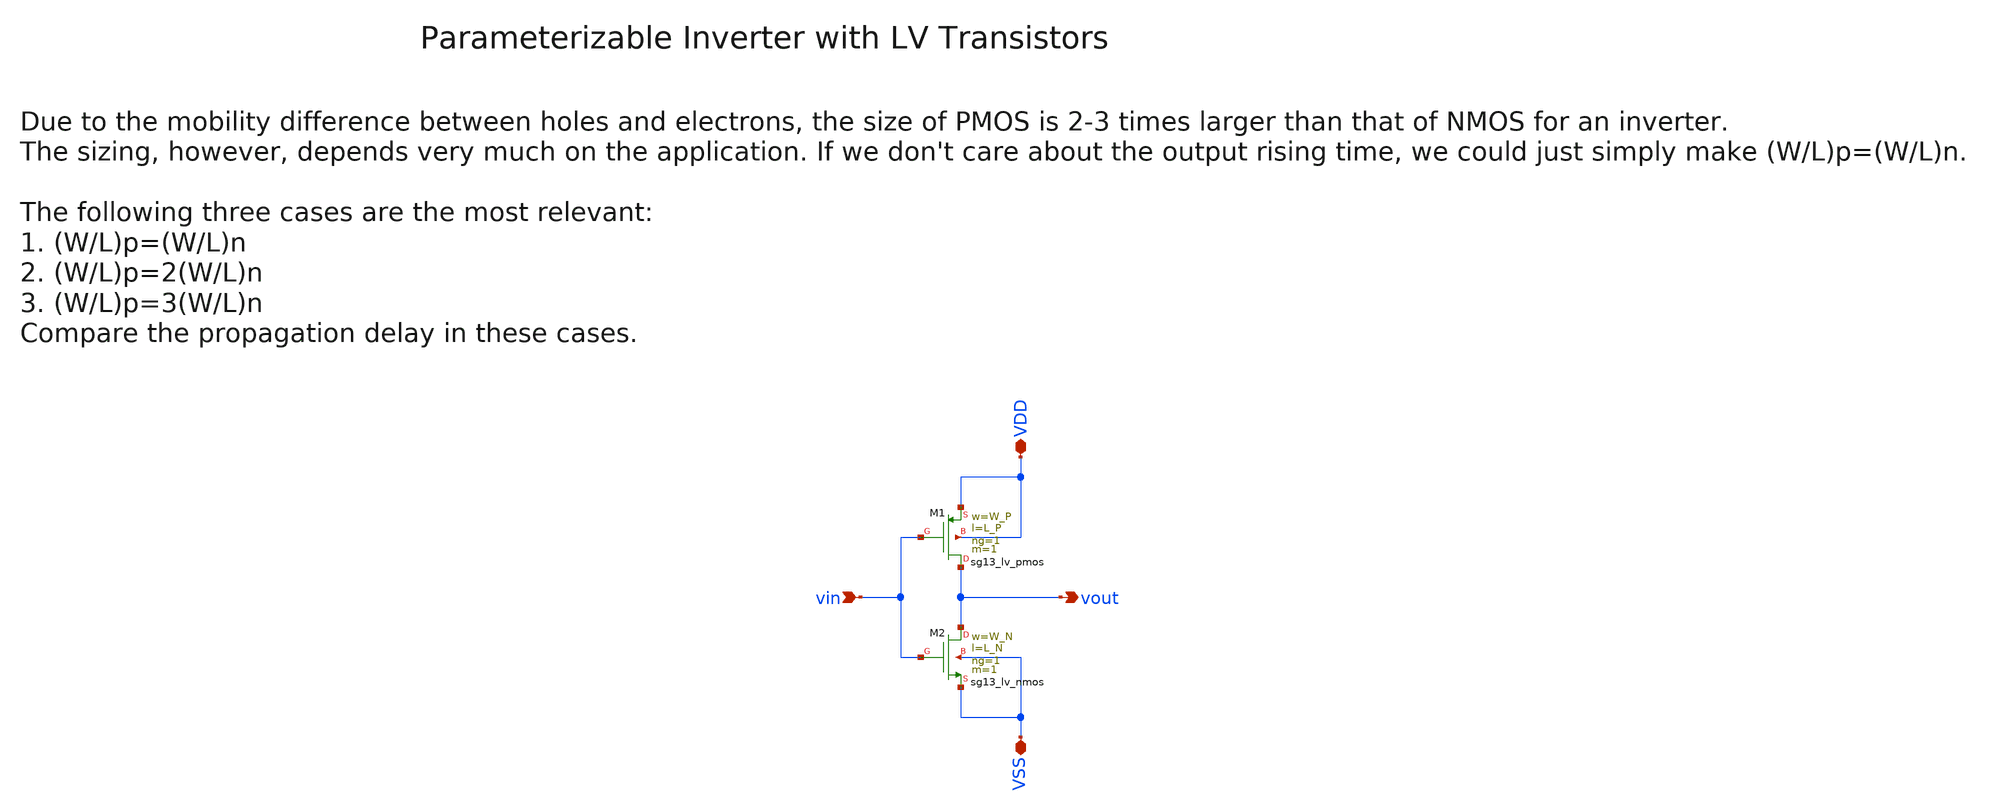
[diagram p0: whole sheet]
** sch_path: SG13G2_ATBS-ADC-main/xschem/inverter/inverter_lv.sch
**.subckt inverter_lv vin VDD VSS vout
*.ipin vin
*.iopin VDD
*.iopin VSS
*.opin vout
XM1 vout vin VDD VDD sg13_lv_pmos w=W_P l=L_P ng=1 m=1 mm_ok=1
XM2 vout vin VSS VSS sg13_lv_nmos w=W_N l=L_N ng=1 m=1 mm_ok=1
**.ends
.end
